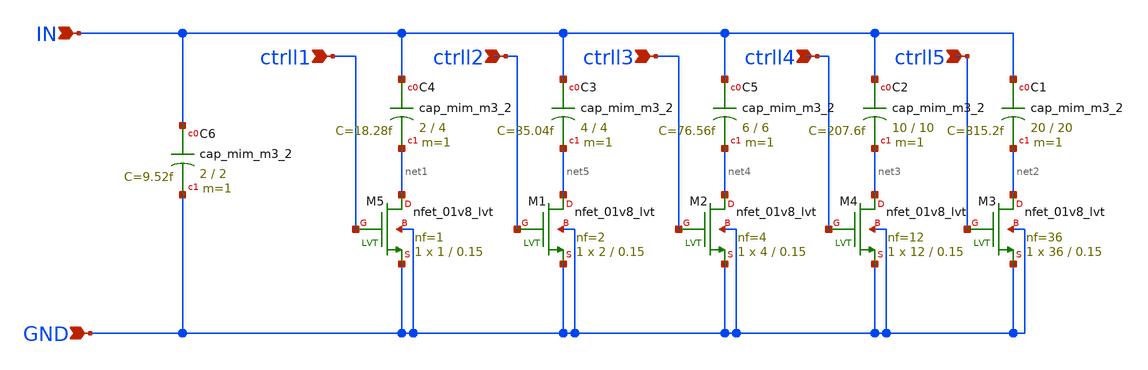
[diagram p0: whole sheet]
** sch_path: design/vco/100M~5G/cap_bank.sch
**.subckt cap_bank IN GND ctrll1 ctrll2 ctrll3 ctrll4 ctrll5
*.ipin IN
*.ipin GND
*.ipin ctrll1
*.ipin ctrll2
*.ipin ctrll3
*.ipin ctrll4
*.ipin ctrll5
XM5 net1 ctrll1 GND GND sky130_fd_pr__nfet_01v8_lvt L=0.15 W=1 nf=1 ad='int((nf+1)/2) * W/nf * 0.29'
+ as='int((nf+2)/2) * W/nf * 0.29' pd='2*int((nf+1)/2) * (W/nf + 0.29)' ps='2*int((nf+2)/2) * (W/nf + 0.29)'
+ nrd='0.29 / W' nrs='0.29 / W' sa=0 sb=0 sd=0 mult=1 m=1
XC4 IN net1 sky130_fd_pr__cap_mim_m3_2 W=2 L=4 MF=1 m=1
XC2 IN net3 sky130_fd_pr__cap_mim_m3_2 W=10 L=10 MF=1 m=1
XC5 IN net4 sky130_fd_pr__cap_mim_m3_2 W=6 L=6 MF=1 m=1
XC3 IN net5 sky130_fd_pr__cap_mim_m3_2 W=4 L=4 MF=1 m=1
XC1 IN net2 sky130_fd_pr__cap_mim_m3_2 W=20 L=20 MF=1 m=1
XC6 IN GND sky130_fd_pr__cap_mim_m3_2 W=2 L=2 MF=1 m=1
XM3 net2 ctrll5 GND GND sky130_fd_pr__nfet_01v8_lvt L=0.15 W=36 nf=36 ad='int((nf+1)/2) * W/nf * 0.29'
+ as='int((nf+2)/2) * W/nf * 0.29' pd='2*int((nf+1)/2) * (W/nf + 0.29)' ps='2*int((nf+2)/2) * (W/nf + 0.29)'
+ nrd='0.29 / W' nrs='0.29 / W' sa=0 sb=0 sd=0 mult=1 m=1
XM2 net4 ctrll3 GND GND sky130_fd_pr__nfet_01v8_lvt L=0.15 W=4 nf=4 ad='int((nf+1)/2) * W/nf * 0.29'
+ as='int((nf+2)/2) * W/nf * 0.29' pd='2*int((nf+1)/2) * (W/nf + 0.29)' ps='2*int((nf+2)/2) * (W/nf + 0.29)'
+ nrd='0.29 / W' nrs='0.29 / W' sa=0 sb=0 sd=0 mult=1 m=1
XM4 net3 ctrll4 GND GND sky130_fd_pr__nfet_01v8_lvt L=0.15 W=12 nf=12 ad='int((nf+1)/2) * W/nf * 0.29'
+ as='int((nf+2)/2) * W/nf * 0.29' pd='2*int((nf+1)/2) * (W/nf + 0.29)' ps='2*int((nf+2)/2) * (W/nf + 0.29)'
+ nrd='0.29 / W' nrs='0.29 / W' sa=0 sb=0 sd=0 mult=1 m=1
XM1 net5 ctrll2 GND GND sky130_fd_pr__nfet_01v8_lvt L=0.15 W=2 nf=2 ad='int((nf+1)/2) * W/nf * 0.29'
+ as='int((nf+2)/2) * W/nf * 0.29' pd='2*int((nf+1)/2) * (W/nf + 0.29)' ps='2*int((nf+2)/2) * (W/nf + 0.29)'
+ nrd='0.29 / W' nrs='0.29 / W' sa=0 sb=0 sd=0 mult=1 m=1
**.ends
.end
